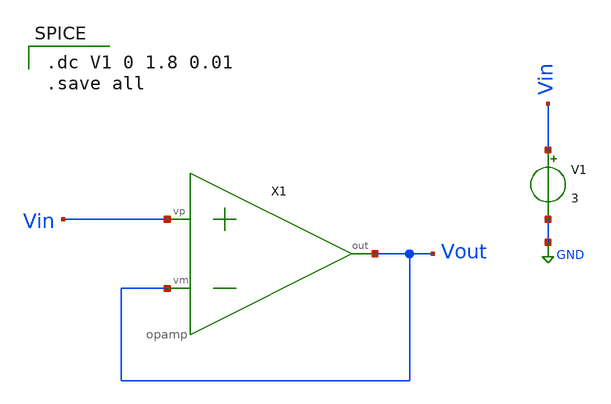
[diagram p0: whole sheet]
** sch_path: xschem/MISC/opamp_TB.sch
**.subckt opamp_TB
X1 Vin Vout Vout opamp
V1 Vin GND 3
**** begin user architecture code

.dc V1 0 1.8 0.01
.save all

**** end user architecture code
**.ends

* expanding   symbol:  opamp.sym # of pins=3
** sym_path: xschem/MISC/opamp.sym
** sch_path: xschem/MISC/opamp.sch
.subckt opamp vp vm out
*.ipin vp
*.ipin vm
*.opin out
E1 out GND vp vm 1E6
.ends

.GLOBAL GND
.end
